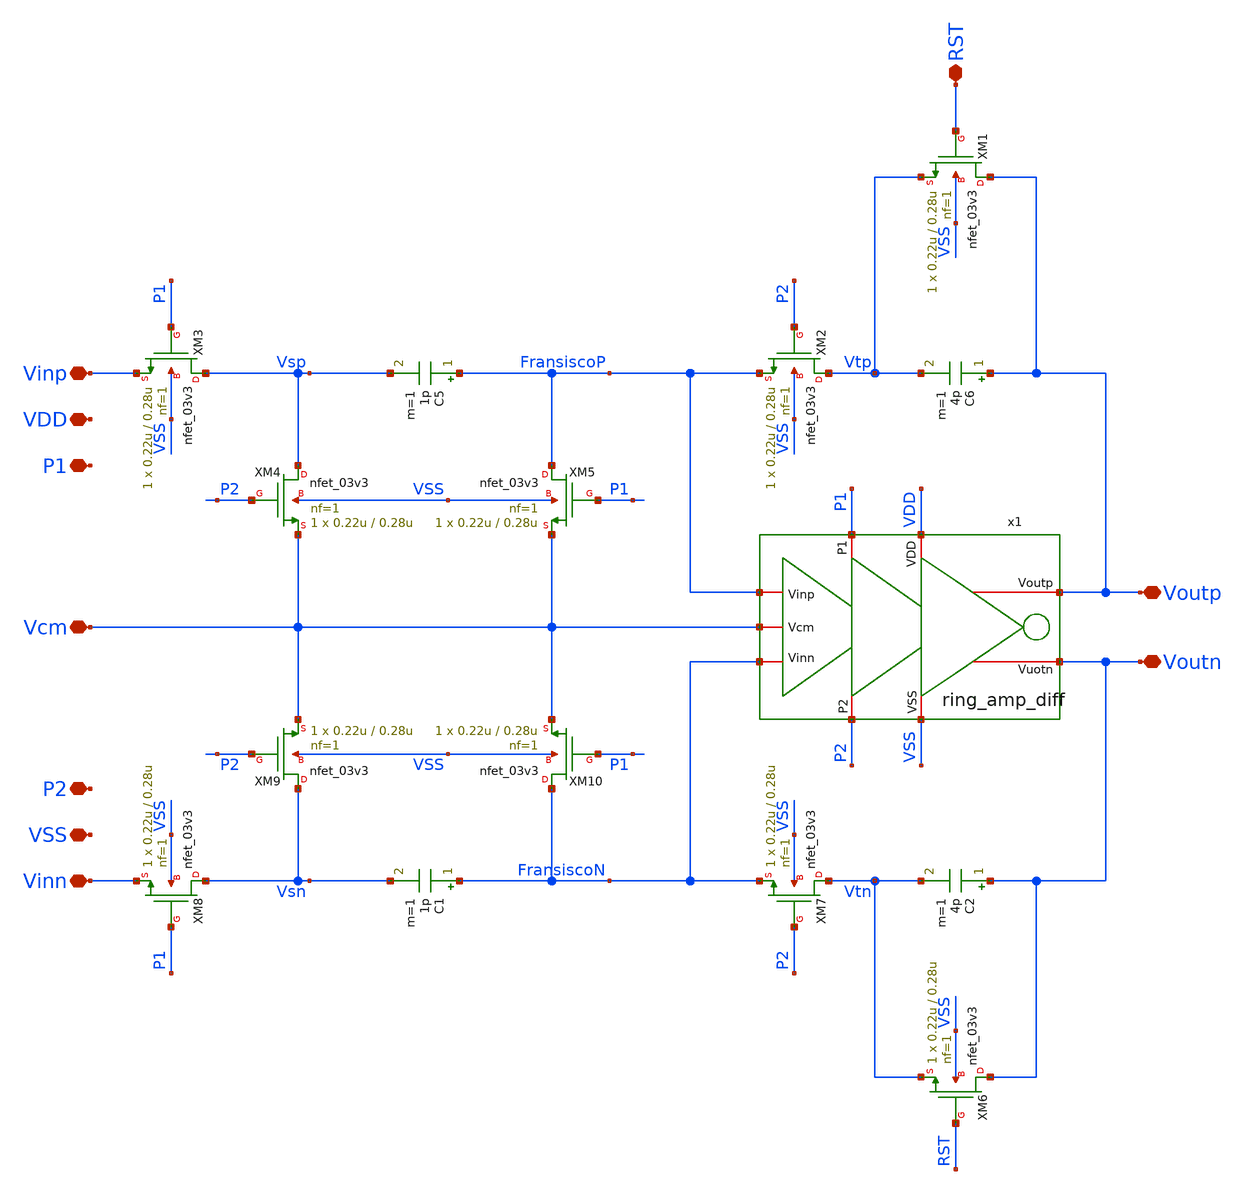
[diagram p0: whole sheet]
** sch_path: designs/DS_modulator/integrator/xschem/integrator.sch
**.subckt integrator Vinp Vcm Vinn Voutp Voutn RST VDD P1 VSS P2
*.iopin Vinp
*.iopin Vcm
*.iopin Vinn
*.iopin Voutp
*.iopin Voutn
*.iopin RST
*.iopin VDD
*.iopin P1
*.iopin VSS
*.iopin P2
XM1 Voutp RST Vtp VSS nfet_03v3 L=0.28u W=0.22u nf=1 ad='int((nf+1)/2) * W/nf * 0.18u' as='int((nf+2)/2) * W/nf * 0.18u'
+ pd='2*int((nf+1)/2) * (W/nf + 0.18u)' ps='2*int((nf+2)/2) * (W/nf + 0.18u)' nrd='0.18u / W' nrs='0.18u / W'
+ sa=0 sb=0 sd=0 m=1
XM2 Vtp P2 FransiscoP VSS nfet_03v3 L=0.28u W=0.22u nf=1 ad='int((nf+1)/2) * W/nf * 0.18u' as='int((nf+2)/2) * W/nf * 0.18u'
+ pd='2*int((nf+1)/2) * (W/nf + 0.18u)' ps='2*int((nf+2)/2) * (W/nf + 0.18u)' nrd='0.18u / W' nrs='0.18u / W'
+ sa=0 sb=0 sd=0 m=1
XM3 Vsp P1 Vinp VSS nfet_03v3 L=0.28u W=0.22u nf=1 ad='int((nf+1)/2) * W/nf * 0.18u' as='int((nf+2)/2) * W/nf * 0.18u'
+ pd='2*int((nf+1)/2) * (W/nf + 0.18u)' ps='2*int((nf+2)/2) * (W/nf + 0.18u)' nrd='0.18u / W' nrs='0.18u / W'
+ sa=0 sb=0 sd=0 m=1
XM4 Vsp P2 Vcm VSS nfet_03v3 L=0.28u W=0.22u nf=1 ad='int((nf+1)/2) * W/nf * 0.18u' as='int((nf+2)/2) * W/nf * 0.18u'
+ pd='2*int((nf+1)/2) * (W/nf + 0.18u)' ps='2*int((nf+2)/2) * (W/nf + 0.18u)' nrd='0.18u / W' nrs='0.18u / W'
+ sa=0 sb=0 sd=0 m=1
XM5 FransiscoP P1 Vcm VSS nfet_03v3 L=0.28u W=0.22u nf=1 ad='int((nf+1)/2) * W/nf * 0.18u' as='int((nf+2)/2) * W/nf * 0.18u'
+ pd='2*int((nf+1)/2) * (W/nf + 0.18u)' ps='2*int((nf+2)/2) * (W/nf + 0.18u)' nrd='0.18u / W' nrs='0.18u / W'
+ sa=0 sb=0 sd=0 m=1
XM6 Voutn RST Vtn VSS nfet_03v3 L=0.28u W=0.22u nf=1 ad='int((nf+1)/2) * W/nf * 0.18u' as='int((nf+2)/2) * W/nf * 0.18u'
+ pd='2*int((nf+1)/2) * (W/nf + 0.18u)' ps='2*int((nf+2)/2) * (W/nf + 0.18u)' nrd='0.18u / W' nrs='0.18u / W'
+ sa=0 sb=0 sd=0 m=1
XM7 Vtn P2 FransiscoN VSS nfet_03v3 L=0.28u W=0.22u nf=1 ad='int((nf+1)/2) * W/nf * 0.18u' as='int((nf+2)/2) * W/nf * 0.18u'
+ pd='2*int((nf+1)/2) * (W/nf + 0.18u)' ps='2*int((nf+2)/2) * (W/nf + 0.18u)' nrd='0.18u / W' nrs='0.18u / W'
+ sa=0 sb=0 sd=0 m=1
XM8 Vsn P1 Vinn VSS nfet_03v3 L=0.28u W=0.22u nf=1 ad='int((nf+1)/2) * W/nf * 0.18u' as='int((nf+2)/2) * W/nf * 0.18u'
+ pd='2*int((nf+1)/2) * (W/nf + 0.18u)' ps='2*int((nf+2)/2) * (W/nf + 0.18u)' nrd='0.18u / W' nrs='0.18u / W'
+ sa=0 sb=0 sd=0 m=1
XM9 Vsn P2 Vcm VSS nfet_03v3 L=0.28u W=0.22u nf=1 ad='int((nf+1)/2) * W/nf * 0.18u' as='int((nf+2)/2) * W/nf * 0.18u'
+ pd='2*int((nf+1)/2) * (W/nf + 0.18u)' ps='2*int((nf+2)/2) * (W/nf + 0.18u)' nrd='0.18u / W' nrs='0.18u / W'
+ sa=0 sb=0 sd=0 m=1
XM10 FransiscoN P1 Vcm VSS nfet_03v3 L=0.28u W=0.22u nf=1 ad='int((nf+1)/2) * W/nf * 0.18u' as='int((nf+2)/2) * W/nf * 0.18u'
+ pd='2*int((nf+1)/2) * (W/nf + 0.18u)' ps='2*int((nf+2)/2) * (W/nf + 0.18u)' nrd='0.18u / W' nrs='0.18u / W'
+ sa=0 sb=0 sd=0 m=1
C5 FransiscoP Vsp 1p m=1
C6 Voutp Vtp 4p m=1
C1 FransiscoN Vsn 1p m=1
C2 Voutn Vtn 4p m=1
x1 P1 P2 VDD VSS FransiscoP Voutp Vcm Voutn FransiscoN ring_amp_diff
**.ends
.end
